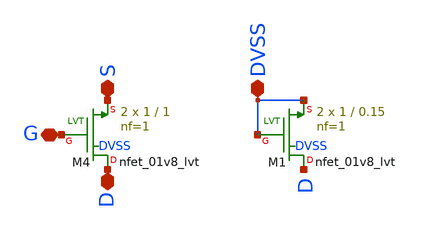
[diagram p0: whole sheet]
** sch_path: magic/vena.sch
**.subckt vena S G D DVSS
*.iopin S
*.iopin G
*.iopin D
*.iopin DVSS
XM4 D G S DVSS sky130_fd_pr__nfet_01v8_lvt L=1 W=1 nf=1 ad='int((nf+1)/2) * W/nf * 0.29' as='int((nf+2)/2) * W/nf * 0.29'
+ pd='2*int((nf+1)/2) * (W/nf + 0.29)' ps='2*int((nf+2)/2) * (W/nf + 0.29)' nrd='0.29 / W' nrs='0.29 / W'
+ sa=0 sb=0 sd=0 mult=2 m=2
XM1 D DVSS DVSS DVSS sky130_fd_pr__nfet_01v8_lvt L=0.15 W=1 nf=1 ad='int((nf+1)/2) * W/nf * 0.29' as='int((nf+2)/2) * W/nf * 0.29'
+ pd='2*int((nf+1)/2) * (W/nf + 0.29)' ps='2*int((nf+2)/2) * (W/nf + 0.29)' nrd='0.29 / W' nrs='0.29 / W'
+ sa=0 sb=0 sd=0 mult=2 m=2
**.ends
.end
